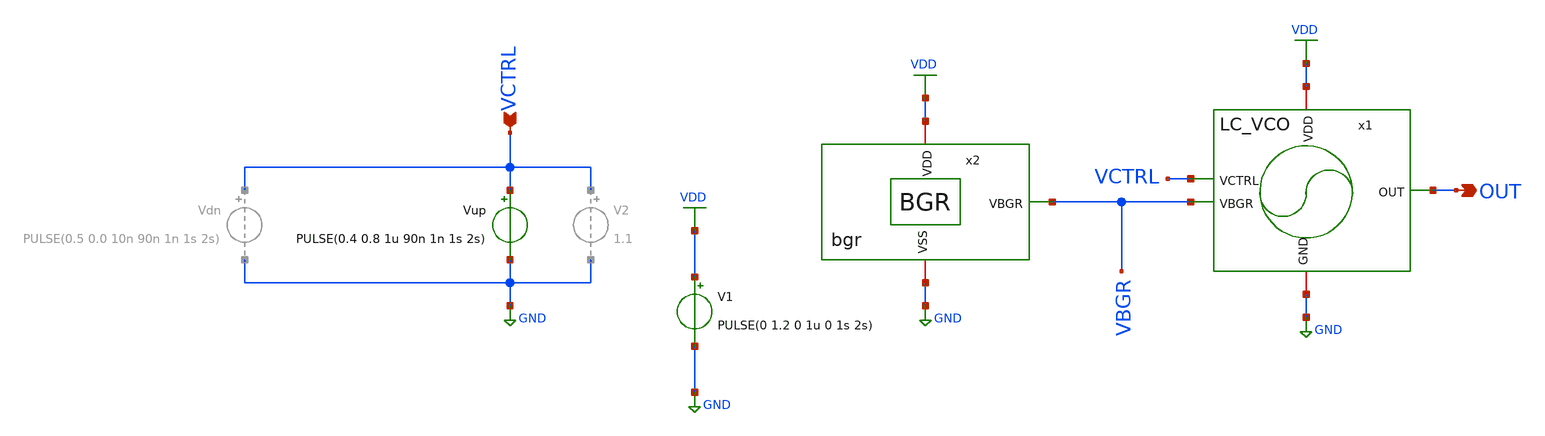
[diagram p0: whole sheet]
** sch_path: schematic/lc-vco/LC_VCO_tb.sch
**.subckt LC_VCO_tb OUT VCTRL
*.opin OUT
*.ipin VCTRL
V1 VDD GND PULSE(0 1.2 0 1u 0 1s 2s)
Vup VCTRL GND PULSE(0.4 0.8 1u 90n 1n 1s 2s)
x1 VDD VCTRL GND OUT VBGR LC_VCO
x2 VBGR VDD GND bgr
**** begin user architecture code



.param temp = 27
.options method=gear rshunt=1.0e12

.control

* Save required signals
save v(VCTRL) v(OUT) v(x1.Vx) v(x1.OUTp) v(VBGR)

* Long transient simulation
tran 10p 2u

* Save raw waveform
write LC_VCO_standalone_tran.raw

* Plot transient waveform
let vout = v(OUT)
plot v(VCTRL) v(x1.Vx) v(OUT) v(x1.OUTp) v(VBGR)
plot v(VBGR)

* Plot steady-state waveform
plot v(VCTRL) v(x1.Vx) v(OUT) v(x1.OUTp) v(VBGR) xlimit 4000n 4005n

* FFT analysis
setplot tran1
linearize vout
set specwindow=blackman
fft vout

* Plot FFT spectrum
let power_out_db = db(vout)
plot power_out_db xlimit 2.34G 2.54G ylimit -200 0

* Find the maximum magnitude value between 2G and 3G
meas sp max_power_out_db max power_out_db FROM=2G TO=3G

* Save FFT spectrum as raw file
write LC_VCO_fft.raw

* Save FFT data
wrdata fft_output_standalone.txt frequency power_out_db

* Save waveform for external processing
wrdata vco_waveform_standalone.txt power_out_db

.endc






.param temp=27
.control
save all
op
write LC_VCO_tb.raw
.endc




.include ../ihp_4nh_inductor.spice


.lib cornerMOSlv.lib mos_tt
.lib cornerMOShv.lib mos_tt
.lib cornerRES.lib res_typ
.lib cornerCAP.lib cap_typ

**** end user architecture code
**.ends
.GLOBAL GND
.GLOBAL VDD
.end
